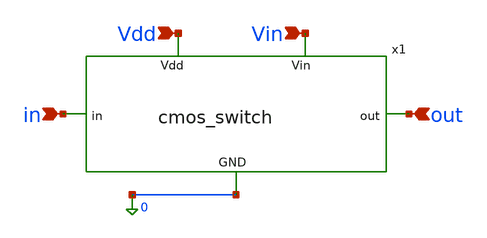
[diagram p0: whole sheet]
** sch_path: MRTMOS_final_chip/cmos_switch_testbench.sch
**.subckt cmos_switch_testbench Vdd Vin in out
*.ipin Vdd
*.ipin Vin
*.ipin in
*.ipin out
x1 Vdd in Vin 0 out cmos_switch
**** begin user architecture code


.include /foss/pdks/gf180mcuD/libs.tech/ngspice/design.ngspice
.lib /foss/pdks/gf180mcuD/libs.tech/ngspice/sm141064.ngspice ff

* ==========================================
* 1. TESTBENCH COMPONENTS (Stimuli & Loads)
* ==========================================
V_Vdd Vdd 0 5
V_ctrl Vin 0 5
V_in_stim in 0 DC 0 PULSE(0 5 0 100p 100p 10u 20u)
I_test out in 0
R_dummy out 0 100Meg

* ---> THE MISSING CAPACITOR <---
C_load out 0 1p

* ==========================================
* 2. AUTOMATED SIMULATION SCRIPT
* ==========================================
.control

  * Color Customization (color2 = 1st trace, color3 = 2nd trace)
  set color0 = black
  set color1 = white
  set color2 = red
  set color3 = green

  * ----------------------------------------
  * TEST 1: TRANSIENT (Delay & Functionality)
  * ----------------------------------------
  alter I_test = 0
  tran 0.1n 20u
  plot v(in) v(out) title 'Test 1: Transient Step Response'

  * ----------------------------------------
  * TEST 2: DC SWEEP (Ron Bathtub Curve)
  * ----------------------------------------
  alter I_test = 1u
  dc V_in_stim 0 5 0.01
  let ron = (v(in) - v(out)) / 1u
  plot ron title 'Test 2: Switch ON-Resistance' ylabel 'Resistance (Ohms)' xlabel 'Input Voltage (V)'

  * ----------------------------------------
  * TEST 3: OFF-STATE LEAKAGE (Blocking Strength)
  * ----------------------------------------
  * 1. Turn the transmission gate completely OFF
  alter V_ctrl = 0
  alter I_test = 0

  * 2. Force the output to 0V by lowering the dummy resistor to 1 milli-ohm
  * This creates the maximum VDS across the switch.
  alter R_dummy = 1e-3

  * 3. Sweep the input voltage from 0V to 5V
  dc V_in_stim 0 5 0.01

  * 4. Measure the current drawn by the input source (absolute value for readability)
  let i_leakage = abs(i(V_in_stim))
  plot i_leakage title 'Test 3: OFF-State Leakage Current' ylabel 'Leakage Current (A)' xlabel 'Input Voltage (V)'

  * ----------------------------------------
  * TEST 4: CHARGE INJECTION & CLOCK FEEDTHROUGH
  * ----------------------------------------
  * 1. Ensure test current is off and dummy resistor is high
  alter I_test = 0
  alter R_dummy = 100Meg

  * 2. Force Input to constant 2.5V (Worst-case for CMOS Tx-Gate)
  alter V_in_stim pulse = [ 2.5 2.5 0 1n 1n 1s 2s ]

  * 3. Pulse the Control pin from 5V (ON) to 0V (OFF) at 5us
  alter V_ctrl pulse = [ 5 0 5u 100p 100p 5u 10u ]

  * 4. Run transient analysis
  tran 10p 10u

  * 5. Plot the exact moment the switch turns OFF
  plot v(in) v(out) xl 4.9u 5.2u title 'Test 4: Charge Injection (Mid-Rail)'

.endc


**** end user architecture code
**.ends

* expanding   symbol:  cmos_switch.sym # of pins=5
** sym_path: MRTMOS_final_chip/cmos_switch.sym
** sch_path: MRTMOS_final_chip/cmos_switch.sch
.subckt cmos_switch Vdd in Vin GND out
*.ipin Vdd
*.ipin Vin
*.ipin in
*.ipin out
*.ipin GND
XM1 in Vin out GND nfet_05v0 L=0.7u W=2u nf=2 ad='int((nf+1)/2) * W/nf * 0.18u' as='int((nf+2)/2) * W/nf * 0.18u'
+ pd='2*int((nf+1)/2) * (W/nf + 0.18u)' ps='2*int((nf+2)/2) * (W/nf + 0.18u)' nrd='0.18u / W' nrs='0.18u / W'
+ sa=0 sb=0 sd=0 m=1
XM2 out net1 in Vdd pfet_05v0 L=0.7u W=6u nf=6 ad='int((nf+1)/2) * W/nf * 0.18u' as='int((nf+2)/2) * W/nf * 0.18u'
+ pd='2*int((nf+1)/2) * (W/nf + 0.18u)' ps='2*int((nf+2)/2) * (W/nf + 0.18u)' nrd='0.18u / W' nrs='0.18u / W'
+ sa=0 sb=0 sd=0 m=1
XM3 net1 Vin GND GND nfet_05v0 L=0.7u W=1u nf=1 ad='int((nf+1)/2) * W/nf * 0.18u' as='int((nf+2)/2) * W/nf * 0.18u'
+ pd='2*int((nf+1)/2) * (W/nf + 0.18u)' ps='2*int((nf+2)/2) * (W/nf + 0.18u)' nrd='0.18u / W' nrs='0.18u / W'
+ sa=0 sb=0 sd=0 m=1
XM4 net1 Vin Vdd Vdd pfet_05v0 L=0.7u W=3u nf=2 ad='int((nf+1)/2) * W/nf * 0.18u' as='int((nf+2)/2) * W/nf * 0.18u'
+ pd='2*int((nf+1)/2) * (W/nf + 0.18u)' ps='2*int((nf+2)/2) * (W/nf + 0.18u)' nrd='0.18u / W' nrs='0.18u / W'
+ sa=0 sb=0 sd=0 m=1
XC3 Vdd GND cap_nmos_06v0 c_width=60e-6 c_length=10e-6 m=6
.ends

.end
